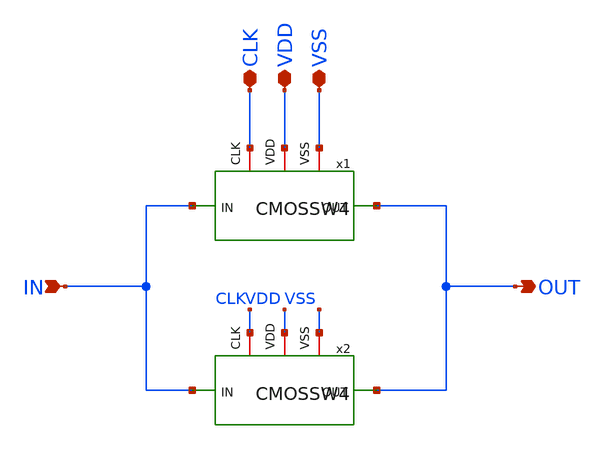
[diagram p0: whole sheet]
** sch_path: CMOSSW8.sch
**.subckt CMOSSW8 IN OUT VSS VDD CLK
*.ipin IN
*.opin OUT
*.iopin VSS
*.iopin VDD
*.iopin CLK
x1 CLK VSS OUT IN VDD CMOSSW4
x2 CLK VSS OUT IN VDD CMOSSW4
**.ends

* expanding   symbol:  C:/Users/ISLab2/Documents/minimal_LR/CMOSSW4.sym # of pins=5
** sym_path: CMOSSW4.sym
** sch_path: CMOSSW4.sch
.subckt CMOSSW4 CLK VSS OUT IN VDD
*.ipin IN
*.opin OUT
*.iopin VSS
*.iopin VDD
*.iopin CLK
x1 CLK VSS OUT IN VDD CMOSSW2
x2 CLK VSS OUT IN VDD CMOSSW2
.ends


* expanding   symbol:  C:/Users/ISLab2/Documents/minimal_LR/CMOSSW2.sym # of pins=5
** sym_path: CMOSSW2.sym
** sch_path: CMOSSW2.sch
.subckt CMOSSW2 CLK VSS OUT IN VDD
*.ipin IN
*.opin OUT
*.iopin VSS
*.iopin VDD
*.iopin CLK
x1 CLK VSS OUT IN VDD CMOSSW
x2 CLK VSS OUT IN VDD CMOSSW
.ends


* expanding   symbol:  C:/Users/ISLab2/Documents/minimal_LR/CMOSSW.sym # of pins=5
** sym_path: CMOSSW.sym
** sch_path: CMOSSW.sch
.subckt CMOSSW CLK VSS OUT IN VDD
*.ipin IN
*.iopin VDD
*.iopin VSS
*.opin OUT
*.iopin CLK
M1 OUT CLK IN VSS nch w=10u l=0.35u as=0 ps=0 ad=0 pd=0 m=1
M2 OUT net1 IN VDD pch w=10u l=0.35u as=0 ps=0 ad=0 pd=0 m=1
**** begin user architecture code


.include C:/Users/ISLab2/Documents/minimal_LR/minimal.txt

**** end user architecture code
x1 VDD net1 CLK VSS INV
.ends


* expanding   symbol:  C:/Users/ISLab2/Documents/minimal_LR/INV.sym # of pins=4
** sym_path: INV.sym
** sch_path: INV.sch
.subckt INV VDD OUT IN VSS
*.opin OUT
*.ipin IN
*.iopin VDD
*.iopin VSS
M2 OUT IN VDD VDD pch w=10u l=0.35u as=0 ps=0 ad=0 pd=0 m=1
M1 OUT IN VSS VSS nch w=5u l=0.35u as=0 ps=0 ad=0 pd=0 m=1
.ends

.end
